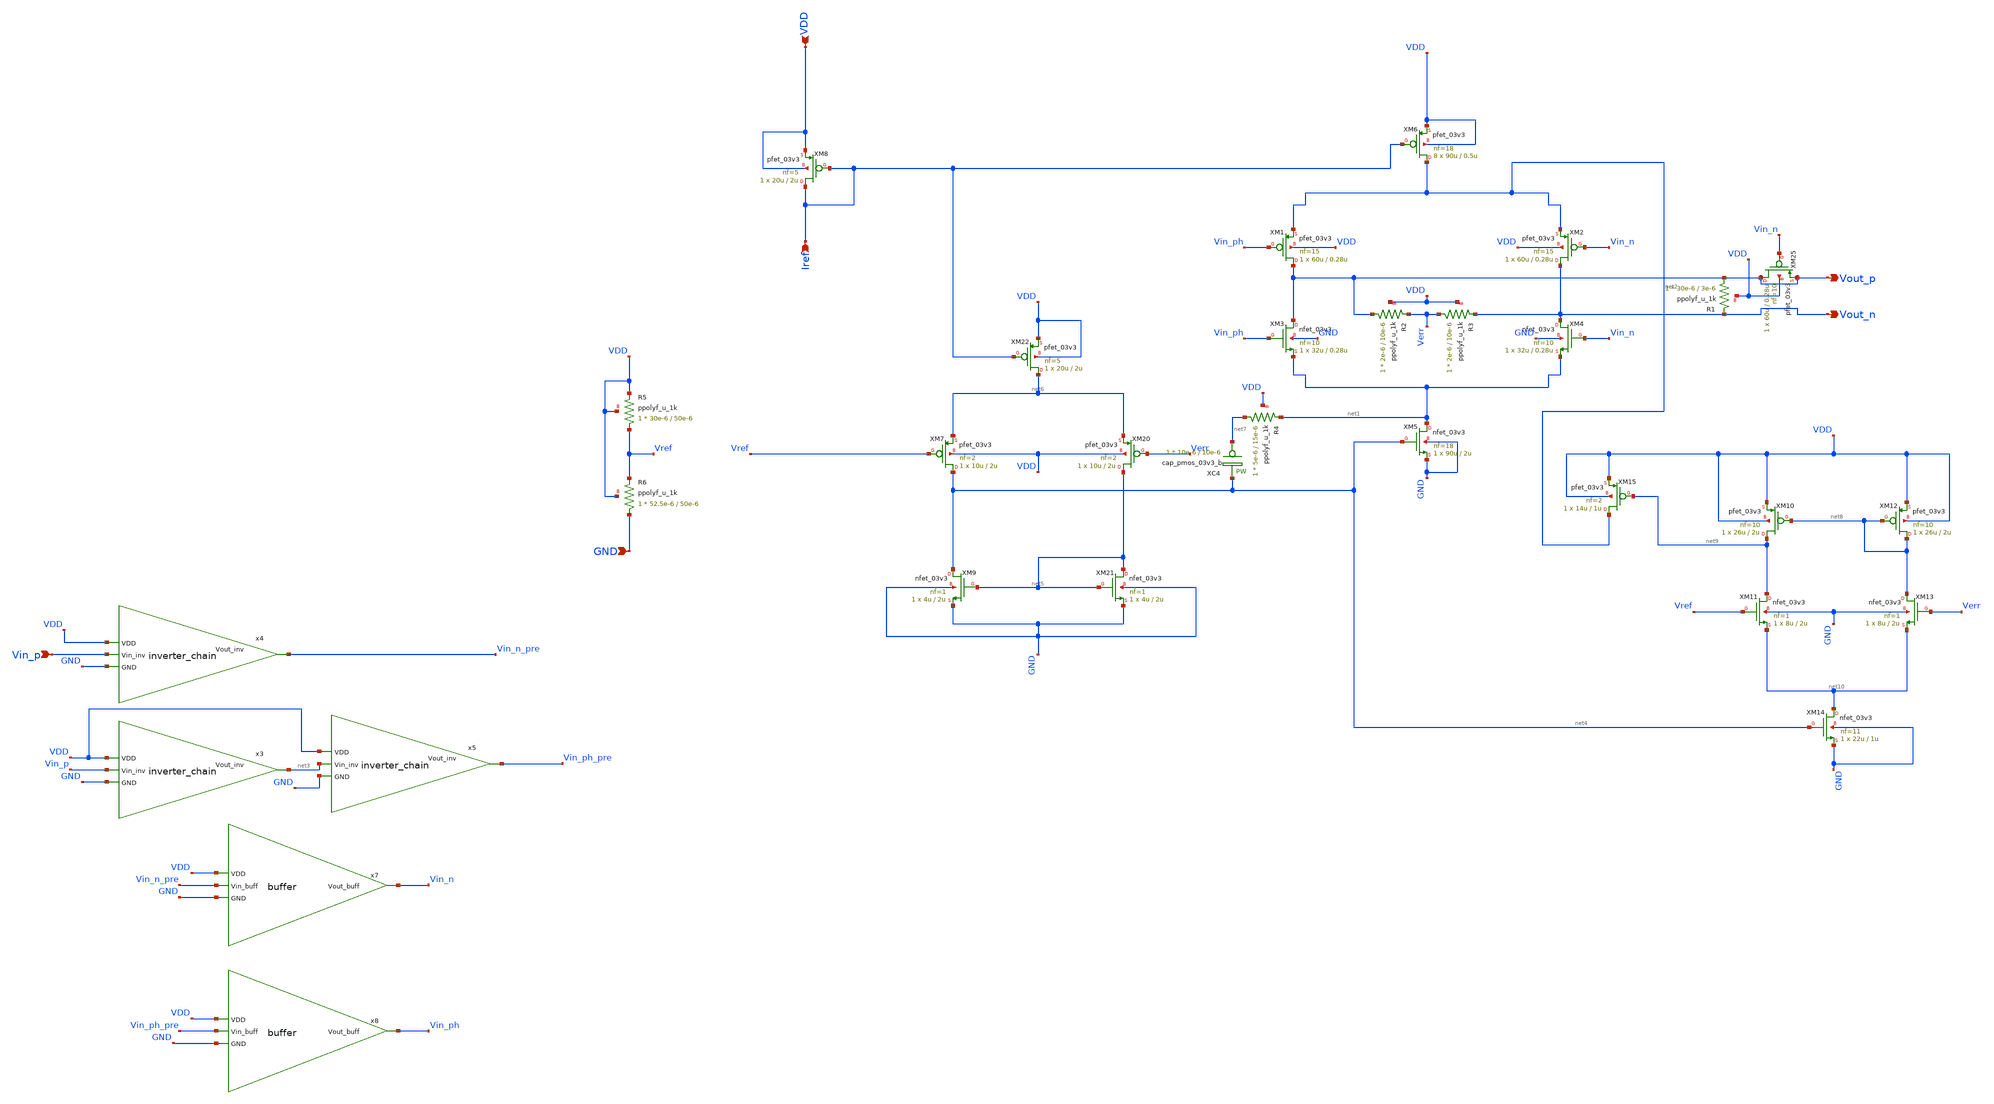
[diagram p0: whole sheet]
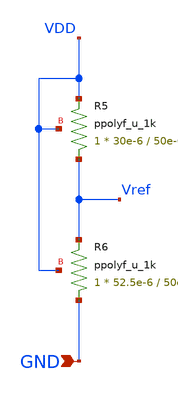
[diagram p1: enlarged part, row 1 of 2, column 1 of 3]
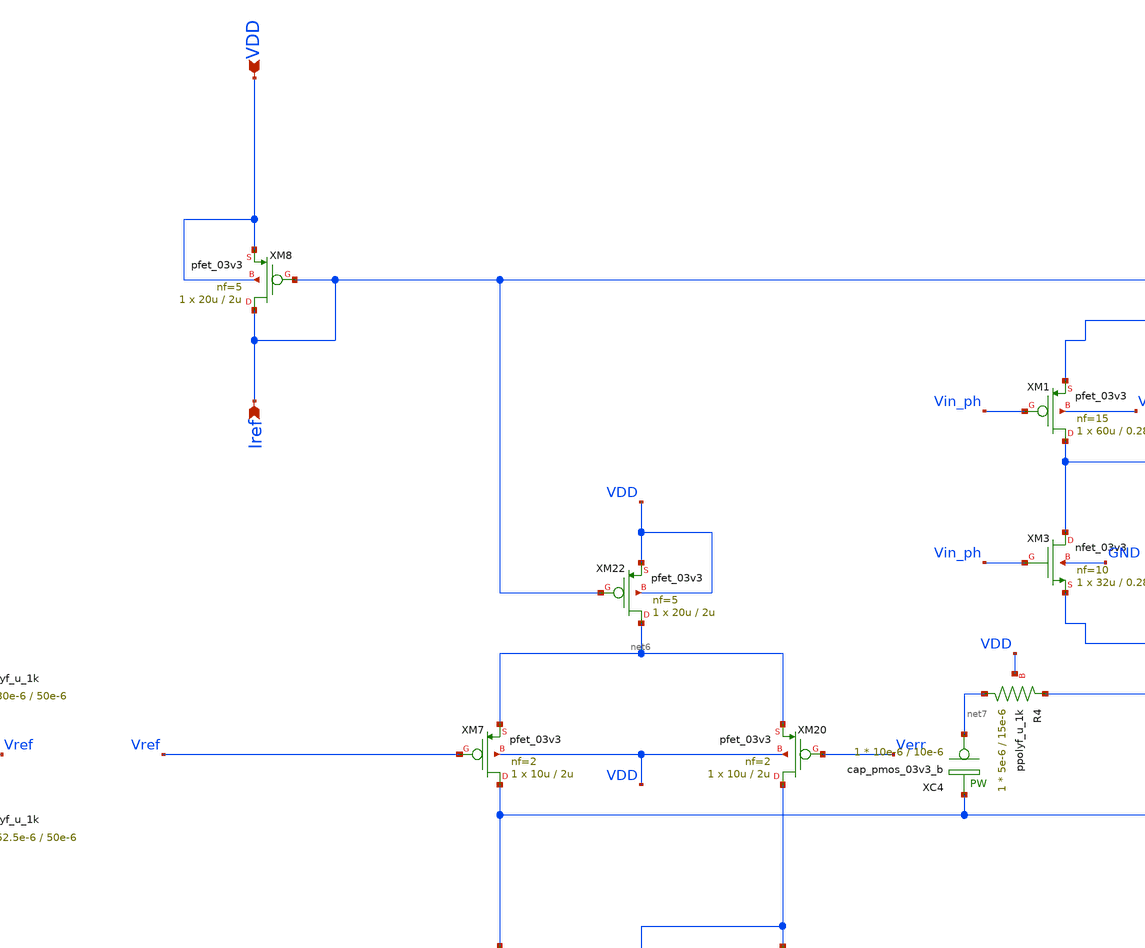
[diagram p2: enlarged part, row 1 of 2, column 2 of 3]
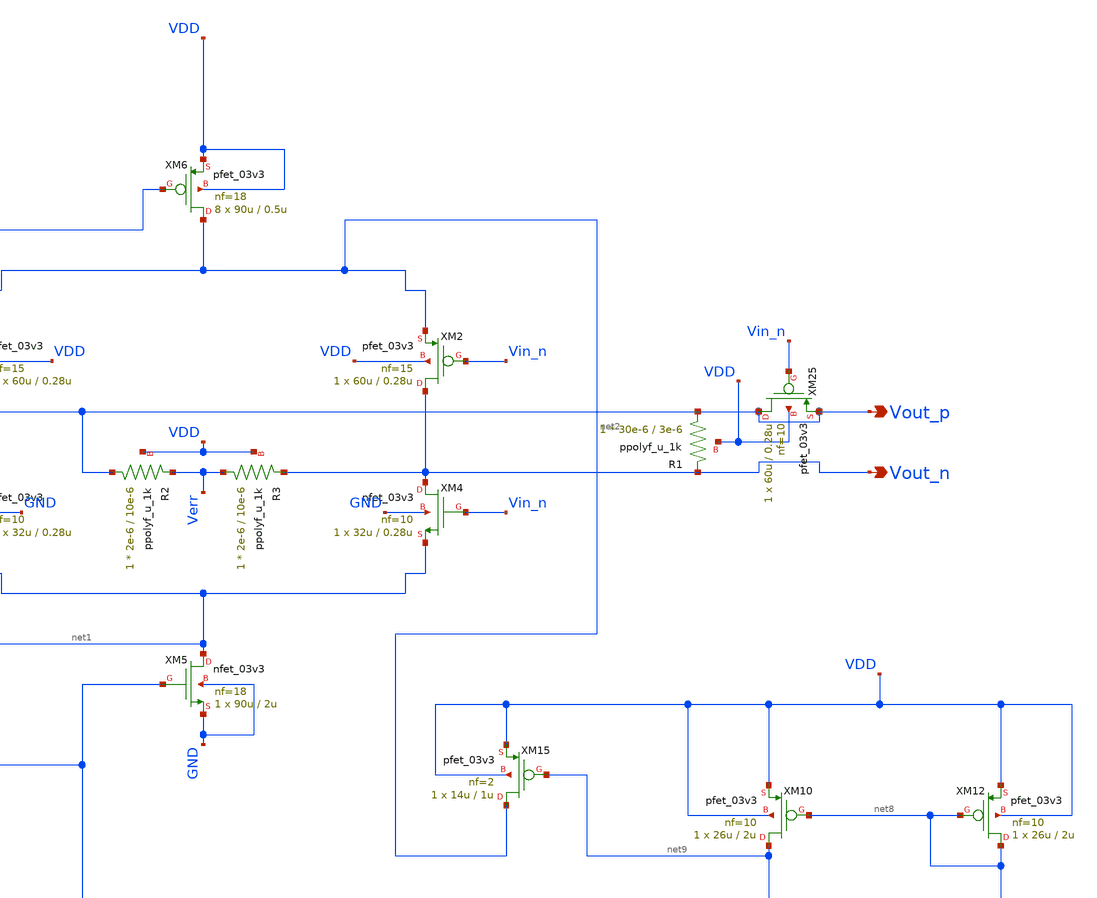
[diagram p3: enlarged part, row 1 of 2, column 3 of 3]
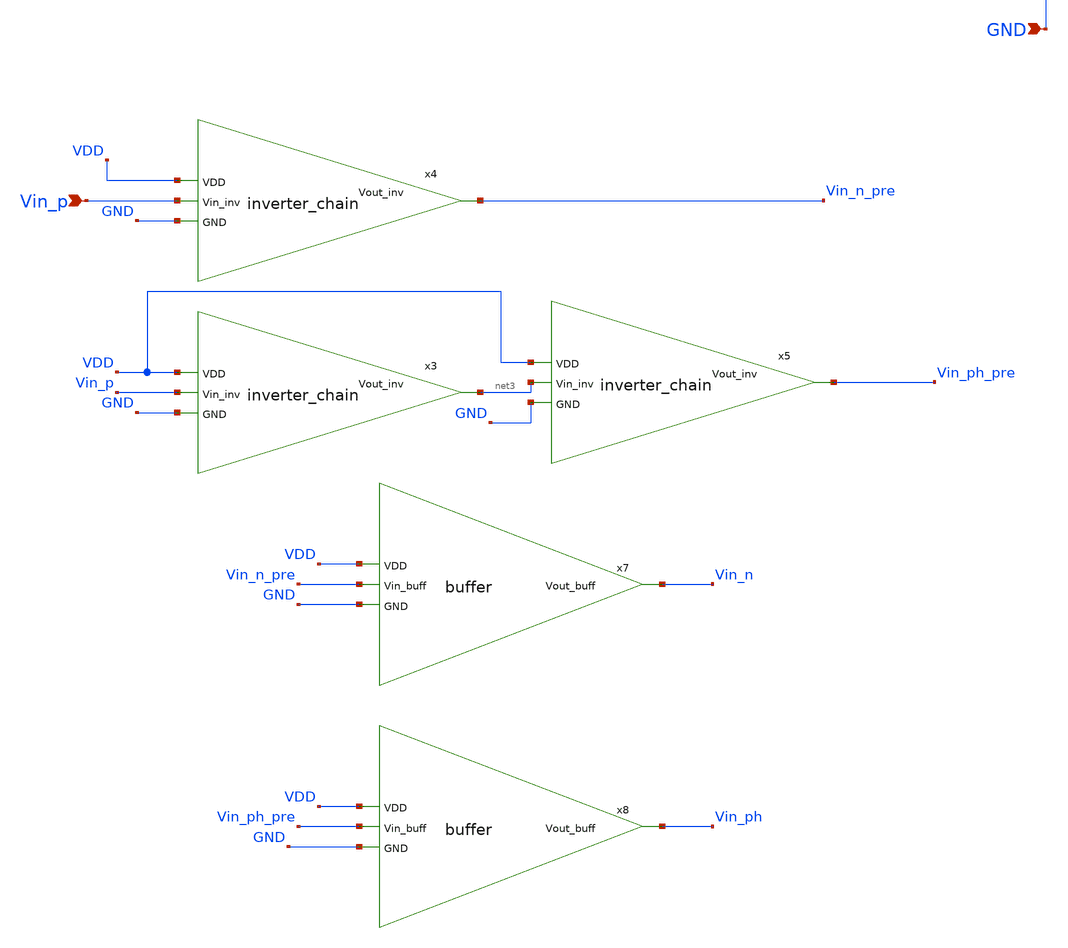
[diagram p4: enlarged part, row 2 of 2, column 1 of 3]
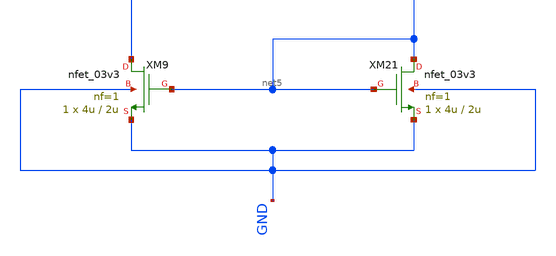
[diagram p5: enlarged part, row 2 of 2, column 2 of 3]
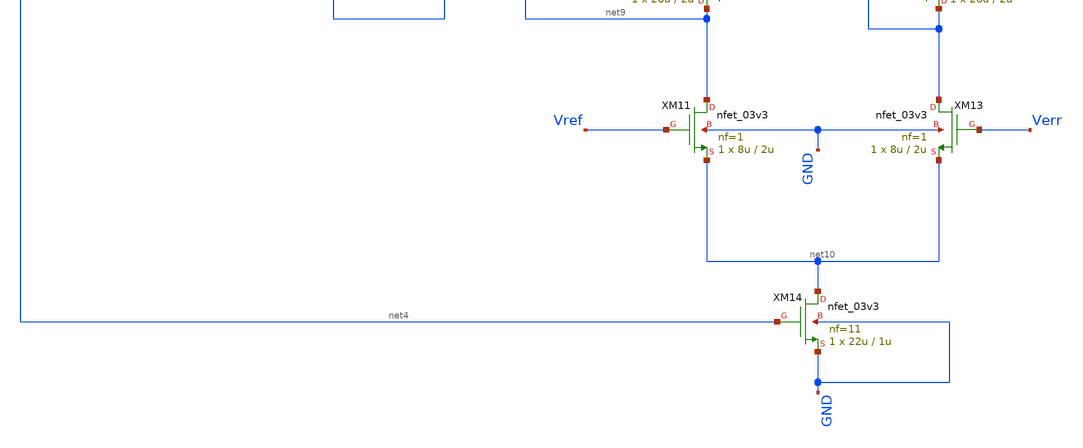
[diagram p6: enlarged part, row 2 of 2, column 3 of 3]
** sch_path: blocks/adc/lvds/lvds_v6.sch
**.subckt lvds_v6 Iref VDD Vout_p Vout_n Vin_p GND
*.ipin Iref
*.ipin VDD
*.opin Vout_p
*.opin Vout_n
*.ipin Vin_p
*.ipin GND
XM1 Vout_p Vin_ph net2 VDD pfet_03v3 L=0.28u W=60u nf=15 ad='int((nf+1)/2) * W/nf * 0.18u' as='int((nf+2)/2) * W/nf * 0.18u'
+ pd='2*int((nf+1)/2) * (W/nf + 0.18u)' ps='2*int((nf+2)/2) * (W/nf + 0.18u)' nrd='0.18u / W' nrs='0.18u / W'
+ sa=0 sb=0 sd=0 m=1
XM2 Vout_n Vin_n net2 VDD pfet_03v3 L=0.28u W=60u nf=15 ad='int((nf+1)/2) * W/nf * 0.18u' as='int((nf+2)/2) * W/nf * 0.18u'
+ pd='2*int((nf+1)/2) * (W/nf + 0.18u)' ps='2*int((nf+2)/2) * (W/nf + 0.18u)' nrd='0.18u / W' nrs='0.18u / W'
+ sa=0 sb=0 sd=0 m=1
XM3 Vout_p Vin_ph net1 GND nfet_03v3 L=0.28u W=32u nf=10 ad='int((nf+1)/2) * W/nf * 0.18u' as='int((nf+2)/2) * W/nf * 0.18u'
+ pd='2*int((nf+1)/2) * (W/nf + 0.18u)' ps='2*int((nf+2)/2) * (W/nf + 0.18u)' nrd='0.18u / W' nrs='0.18u / W'
+ sa=0 sb=0 sd=0 m=1
XM4 Vout_n Vin_n net1 GND nfet_03v3 L=0.28u W=32u nf=10 ad='int((nf+1)/2) * W/nf * 0.18u' as='int((nf+2)/2) * W/nf * 0.18u'
+ pd='2*int((nf+1)/2) * (W/nf + 0.18u)' ps='2*int((nf+2)/2) * (W/nf + 0.18u)' nrd='0.18u / W' nrs='0.18u / W'
+ sa=0 sb=0 sd=0 m=1
XM5 net1 net4 GND GND nfet_03v3 L=2u W=90u nf=18 ad='int((nf+1)/2) * W/nf * 0.18u' as='int((nf+2)/2) * W/nf * 0.18u'
+ pd='2*int((nf+1)/2) * (W/nf + 0.18u)' ps='2*int((nf+2)/2) * (W/nf + 0.18u)' nrd='0.18u / W' nrs='0.18u / W'
+ sa=0 sb=0 sd=0 m=1
XM6 net2 Iref VDD VDD pfet_03v3 L=0.5u W=90u nf=18 ad='int((nf+1)/2) * W/nf * 0.18u' as='int((nf+2)/2) * W/nf * 0.18u'
+ pd='2*int((nf+1)/2) * (W/nf + 0.18u)' ps='2*int((nf+2)/2) * (W/nf + 0.18u)' nrd='0.18u / W' nrs='0.18u / W'
+ sa=0 sb=0 sd=0 m=8
XM8 Iref Iref VDD VDD pfet_03v3 L=2u W=20u nf=5 ad='int((nf+1)/2) * W/nf * 0.18u' as='int((nf+2)/2) * W/nf * 0.18u'
+ pd='2*int((nf+1)/2) * (W/nf + 0.18u)' ps='2*int((nf+2)/2) * (W/nf + 0.18u)' nrd='0.18u / W' nrs='0.18u / W'
+ sa=0 sb=0 sd=0 m=1
XR2 Vout_p Verr VDD ppolyf_u_1k r_width=2e-6 r_length=10e-6 m=1
XR3 Verr Vout_n VDD ppolyf_u_1k r_width=2e-6 r_length=10e-6 m=1
x4 VDD Vin_p Vin_n_pre GND inverter_chain
x3 VDD Vin_p net3 GND inverter_chain
x5 VDD net3 Vin_ph_pre GND inverter_chain
x7 VDD Vin_n Vin_n_pre GND buffer
x8 VDD Vin_ph Vin_ph_pre GND buffer
XR5 Vref VDD VDD ppolyf_u_1k r_width=30e-6 r_length=50e-6 m=1
XR6 GND Vref VDD ppolyf_u_1k r_width=52.5e-6 r_length=50e-6 m=1
XM7 net4 Vref net6 VDD pfet_03v3 L=2u W=10u nf=2 ad='int((nf+1)/2) * W/nf * 0.18u' as='int((nf+2)/2) * W/nf * 0.18u'
+ pd='2*int((nf+1)/2) * (W/nf + 0.18u)' ps='2*int((nf+2)/2) * (W/nf + 0.18u)' nrd='0.18u / W' nrs='0.18u / W'
+ sa=0 sb=0 sd=0 m=1
XM9 net4 net5 GND GND nfet_03v3 L=2u W=4u nf=1 ad='int((nf+1)/2) * W/nf * 0.18u' as='int((nf+2)/2) * W/nf * 0.18u'
+ pd='2*int((nf+1)/2) * (W/nf + 0.18u)' ps='2*int((nf+2)/2) * (W/nf + 0.18u)' nrd='0.18u / W' nrs='0.18u / W'
+ sa=0 sb=0 sd=0 m=1
XM20 net5 Verr net6 VDD pfet_03v3 L=2u W=10u nf=2 ad='int((nf+1)/2) * W/nf * 0.18u' as='int((nf+2)/2) * W/nf * 0.18u'
+ pd='2*int((nf+1)/2) * (W/nf + 0.18u)' ps='2*int((nf+2)/2) * (W/nf + 0.18u)' nrd='0.18u / W' nrs='0.18u / W'
+ sa=0 sb=0 sd=0 m=1
XM21 net5 net5 GND GND nfet_03v3 L=2u W=4u nf=1 ad='int((nf+1)/2) * W/nf * 0.18u' as='int((nf+2)/2) * W/nf * 0.18u'
+ pd='2*int((nf+1)/2) * (W/nf + 0.18u)' ps='2*int((nf+2)/2) * (W/nf + 0.18u)' nrd='0.18u / W' nrs='0.18u / W'
+ sa=0 sb=0 sd=0 m=1
XM22 net6 Iref VDD VDD pfet_03v3 L=2u W=20u nf=5 ad='int((nf+1)/2) * W/nf * 0.18u' as='int((nf+2)/2) * W/nf * 0.18u'
+ pd='2*int((nf+1)/2) * (W/nf + 0.18u)' ps='2*int((nf+2)/2) * (W/nf + 0.18u)' nrd='0.18u / W' nrs='0.18u / W'
+ sa=0 sb=0 sd=0 m=1
XC4 net7 net4 cap_pmos_03v3_b c_width=10e-6 c_length=10e-6 m=1
XR4 net7 net1 VDD ppolyf_u_1k r_width=5e-6 r_length=15e-6 m=1
XM25 Vout_p Vin_n Vout_p VDD pfet_03v3 L=0.28u W=60u nf=10 ad='int((nf+1)/2) * W/nf * 0.18u' as='int((nf+2)/2) * W/nf * 0.18u'
+ pd='2*int((nf+1)/2) * (W/nf + 0.18u)' ps='2*int((nf+2)/2) * (W/nf + 0.18u)' nrd='0.18u / W' nrs='0.18u / W'
+ sa=0 sb=0 sd=0 m=1
XM10 net9 net8 VDD VDD pfet_03v3 L=2u W=26u nf=10 ad='int((nf+1)/2) * W/nf * 0.18u' as='int((nf+2)/2) * W/nf * 0.18u'
+ pd='2*int((nf+1)/2) * (W/nf + 0.18u)' ps='2*int((nf+2)/2) * (W/nf + 0.18u)' nrd='0.18u / W' nrs='0.18u / W'
+ sa=0 sb=0 sd=0 m=1
XM11 net9 Vref net10 GND nfet_03v3 L=2u W=8u nf=1 ad='int((nf+1)/2) * W/nf * 0.18u' as='int((nf+2)/2) * W/nf * 0.18u'
+ pd='2*int((nf+1)/2) * (W/nf + 0.18u)' ps='2*int((nf+2)/2) * (W/nf + 0.18u)' nrd='0.18u / W' nrs='0.18u / W'
+ sa=0 sb=0 sd=0 m=1
XM12 net8 net8 VDD VDD pfet_03v3 L=2u W=26u nf=10 ad='int((nf+1)/2) * W/nf * 0.18u' as='int((nf+2)/2) * W/nf * 0.18u'
+ pd='2*int((nf+1)/2) * (W/nf + 0.18u)' ps='2*int((nf+2)/2) * (W/nf + 0.18u)' nrd='0.18u / W' nrs='0.18u / W'
+ sa=0 sb=0 sd=0 m=1
XM13 net8 Verr net10 GND nfet_03v3 L=2u W=8u nf=1 ad='int((nf+1)/2) * W/nf * 0.18u' as='int((nf+2)/2) * W/nf * 0.18u'
+ pd='2*int((nf+1)/2) * (W/nf + 0.18u)' ps='2*int((nf+2)/2) * (W/nf + 0.18u)' nrd='0.18u / W' nrs='0.18u / W'
+ sa=0 sb=0 sd=0 m=1
XM14 net10 net4 GND GND nfet_03v3 L=1u W=22u nf=11 ad='int((nf+1)/2) * W/nf * 0.18u' as='int((nf+2)/2) * W/nf * 0.18u'
+ pd='2*int((nf+1)/2) * (W/nf + 0.18u)' ps='2*int((nf+2)/2) * (W/nf + 0.18u)' nrd='0.18u / W' nrs='0.18u / W'
+ sa=0 sb=0 sd=0 m=1
XM15 net2 net9 VDD VDD pfet_03v3 L=1u W=14u nf=2 ad='int((nf+1)/2) * W/nf * 0.18u' as='int((nf+2)/2) * W/nf * 0.18u'
+ pd='2*int((nf+1)/2) * (W/nf + 0.18u)' ps='2*int((nf+2)/2) * (W/nf + 0.18u)' nrd='0.18u / W' nrs='0.18u / W'
+ sa=0 sb=0 sd=0 m=1
XR1 Vout_p Vout_n VDD ppolyf_u_1k r_width=30e-6 r_length=3e-6 m=1
**.ends

* expanding   symbol:  inverter_chain.sym # of pins=4
** sym_path: blocks/adc/lvds/inverter_chain.sym
** sch_path: blocks/adc/lvds/inverter_chain.sch
.subckt inverter_chain VDD Vin_inv Vout_inv GND
*.ipin Vin_inv
*.opin Vout_inv
*.ipin VDD
*.ipin GND
XM1 Vout_inv Vin_inv VDD VDD pfet_03v3 L=0.28u W=0.66u nf=1 ad='int((nf+1)/2) * W/nf * 0.18u' as='int((nf+2)/2) * W/nf * 0.18u'
+ pd='2*int((nf+1)/2) * (W/nf + 0.18u)' ps='2*int((nf+2)/2) * (W/nf + 0.18u)' nrd='0.18u / W' nrs='0.18u / W'
+ sa=0 sb=0 sd=0 m=1
XM2 Vout_inv Vin_inv GND GND nfet_03v3 L=0.28u W=0.3u nf=1 ad='int((nf+1)/2) * W/nf * 0.18u' as='int((nf+2)/2) * W/nf * 0.18u'
+ pd='2*int((nf+1)/2) * (W/nf + 0.18u)' ps='2*int((nf+2)/2) * (W/nf + 0.18u)' nrd='0.18u / W' nrs='0.18u / W'
+ sa=0 sb=0 sd=0 m=1
.ends


* expanding   symbol:  buffer.sym # of pins=4
** sym_path: blocks/adc/lvds/buffer.sym
** sch_path: blocks/adc/lvds/buffer.sch
.subckt buffer VDD Vout_buff Vin_buff GND
*.ipin VDD
*.ipin Vin_buff
*.opin Vout_buff
*.ipin GND
XM1 net1 Vin_buff VDD VDD pfet_03v3 L=0.28u W=0.66u nf=1 ad='int((nf+1)/2) * W/nf * 0.18u' as='int((nf+2)/2) * W/nf * 0.18u'
+ pd='2*int((nf+1)/2) * (W/nf + 0.18u)' ps='2*int((nf+2)/2) * (W/nf + 0.18u)' nrd='0.18u / W' nrs='0.18u / W'
+ sa=0 sb=0 sd=0 m=1
XM2 net1 Vin_buff GND GND nfet_03v3 L=0.28u W=0.3u nf=1 ad='int((nf+1)/2) * W/nf * 0.18u' as='int((nf+2)/2) * W/nf * 0.18u'
+ pd='2*int((nf+1)/2) * (W/nf + 0.18u)' ps='2*int((nf+2)/2) * (W/nf + 0.18u)' nrd='0.18u / W' nrs='0.18u / W'
+ sa=0 sb=0 sd=0 m=1
XM3 net2 net1 VDD VDD pfet_03v3 L=0.28u W=2.64u nf=1 ad='int((nf+1)/2) * W/nf * 0.18u' as='int((nf+2)/2) * W/nf * 0.18u'
+ pd='2*int((nf+1)/2) * (W/nf + 0.18u)' ps='2*int((nf+2)/2) * (W/nf + 0.18u)' nrd='0.18u / W' nrs='0.18u / W'
+ sa=0 sb=0 sd=0 m=1
XM4 net2 net1 GND GND nfet_03v3 L=0.28u W=0.88u nf=1 ad='int((nf+1)/2) * W/nf * 0.18u' as='int((nf+2)/2) * W/nf * 0.18u'
+ pd='2*int((nf+1)/2) * (W/nf + 0.18u)' ps='2*int((nf+2)/2) * (W/nf + 0.18u)' nrd='0.18u / W' nrs='0.18u / W'
+ sa=0 sb=0 sd=0 m=1
XM5 net3 net2 VDD VDD pfet_03v3 L=0.28u W=10.56u nf=1 ad='int((nf+1)/2) * W/nf * 0.18u' as='int((nf+2)/2) * W/nf * 0.18u'
+ pd='2*int((nf+1)/2) * (W/nf + 0.18u)' ps='2*int((nf+2)/2) * (W/nf + 0.18u)' nrd='0.18u / W' nrs='0.18u / W'
+ sa=0 sb=0 sd=0 m=1
XM6 net3 net2 GND GND nfet_03v3 L=0.28u W=3.52u nf=1 ad='int((nf+1)/2) * W/nf * 0.18u' as='int((nf+2)/2) * W/nf * 0.18u'
+ pd='2*int((nf+1)/2) * (W/nf + 0.18u)' ps='2*int((nf+2)/2) * (W/nf + 0.18u)' nrd='0.18u / W' nrs='0.18u / W'
+ sa=0 sb=0 sd=0 m=1
XM7 Vout_buff net3 VDD VDD pfet_03v3 L=0.28u W=45u nf=15 ad='int((nf+1)/2) * W/nf * 0.18u' as='int((nf+2)/2) * W/nf * 0.18u'
+ pd='2*int((nf+1)/2) * (W/nf + 0.18u)' ps='2*int((nf+2)/2) * (W/nf + 0.18u)' nrd='0.18u / W' nrs='0.18u / W'
+ sa=0 sb=0 sd=0 m=1
XM8 Vout_buff net3 GND GND nfet_03v3 L=0.28u W=14u nf=7 ad='int((nf+1)/2) * W/nf * 0.18u' as='int((nf+2)/2) * W/nf * 0.18u'
+ pd='2*int((nf+1)/2) * (W/nf + 0.18u)' ps='2*int((nf+2)/2) * (W/nf + 0.18u)' nrd='0.18u / W' nrs='0.18u / W'
+ sa=0 sb=0 sd=0 m=1
.ends

.end
